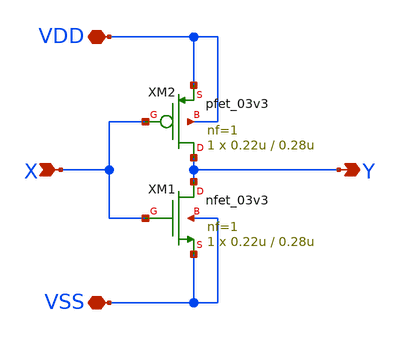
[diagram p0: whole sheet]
** sch_path: designs/analog_test/inv.sch
**.subckt inv Y X VDD VSS
*.opin Y
*.ipin X
*.iopin VDD
*.iopin VSS
XM1 Y X VSS VSS nfet_03v3 L=0.28u W=0.22u nf=1 ad='int((nf+1)/2) * W/nf * 0.18u' as='int((nf+2)/2) * W/nf * 0.18u'
+ pd='2*int((nf+1)/2) * (W/nf + 0.18u)' ps='2*int((nf+2)/2) * (W/nf + 0.18u)' nrd='0.18u / W' nrs='0.18u / W'
+ sa=0 sb=0 sd=0 m=1
XM2 Y X VDD VDD pfet_03v3 L=0.28u W=0.22u nf=1 ad='int((nf+1)/2) * W/nf * 0.18u' as='int((nf+2)/2) * W/nf * 0.18u'
+ pd='2*int((nf+1)/2) * (W/nf + 0.18u)' ps='2*int((nf+2)/2) * (W/nf + 0.18u)' nrd='0.18u / W' nrs='0.18u / W'
+ sa=0 sb=0 sd=0 m=1
**.ends
.end
